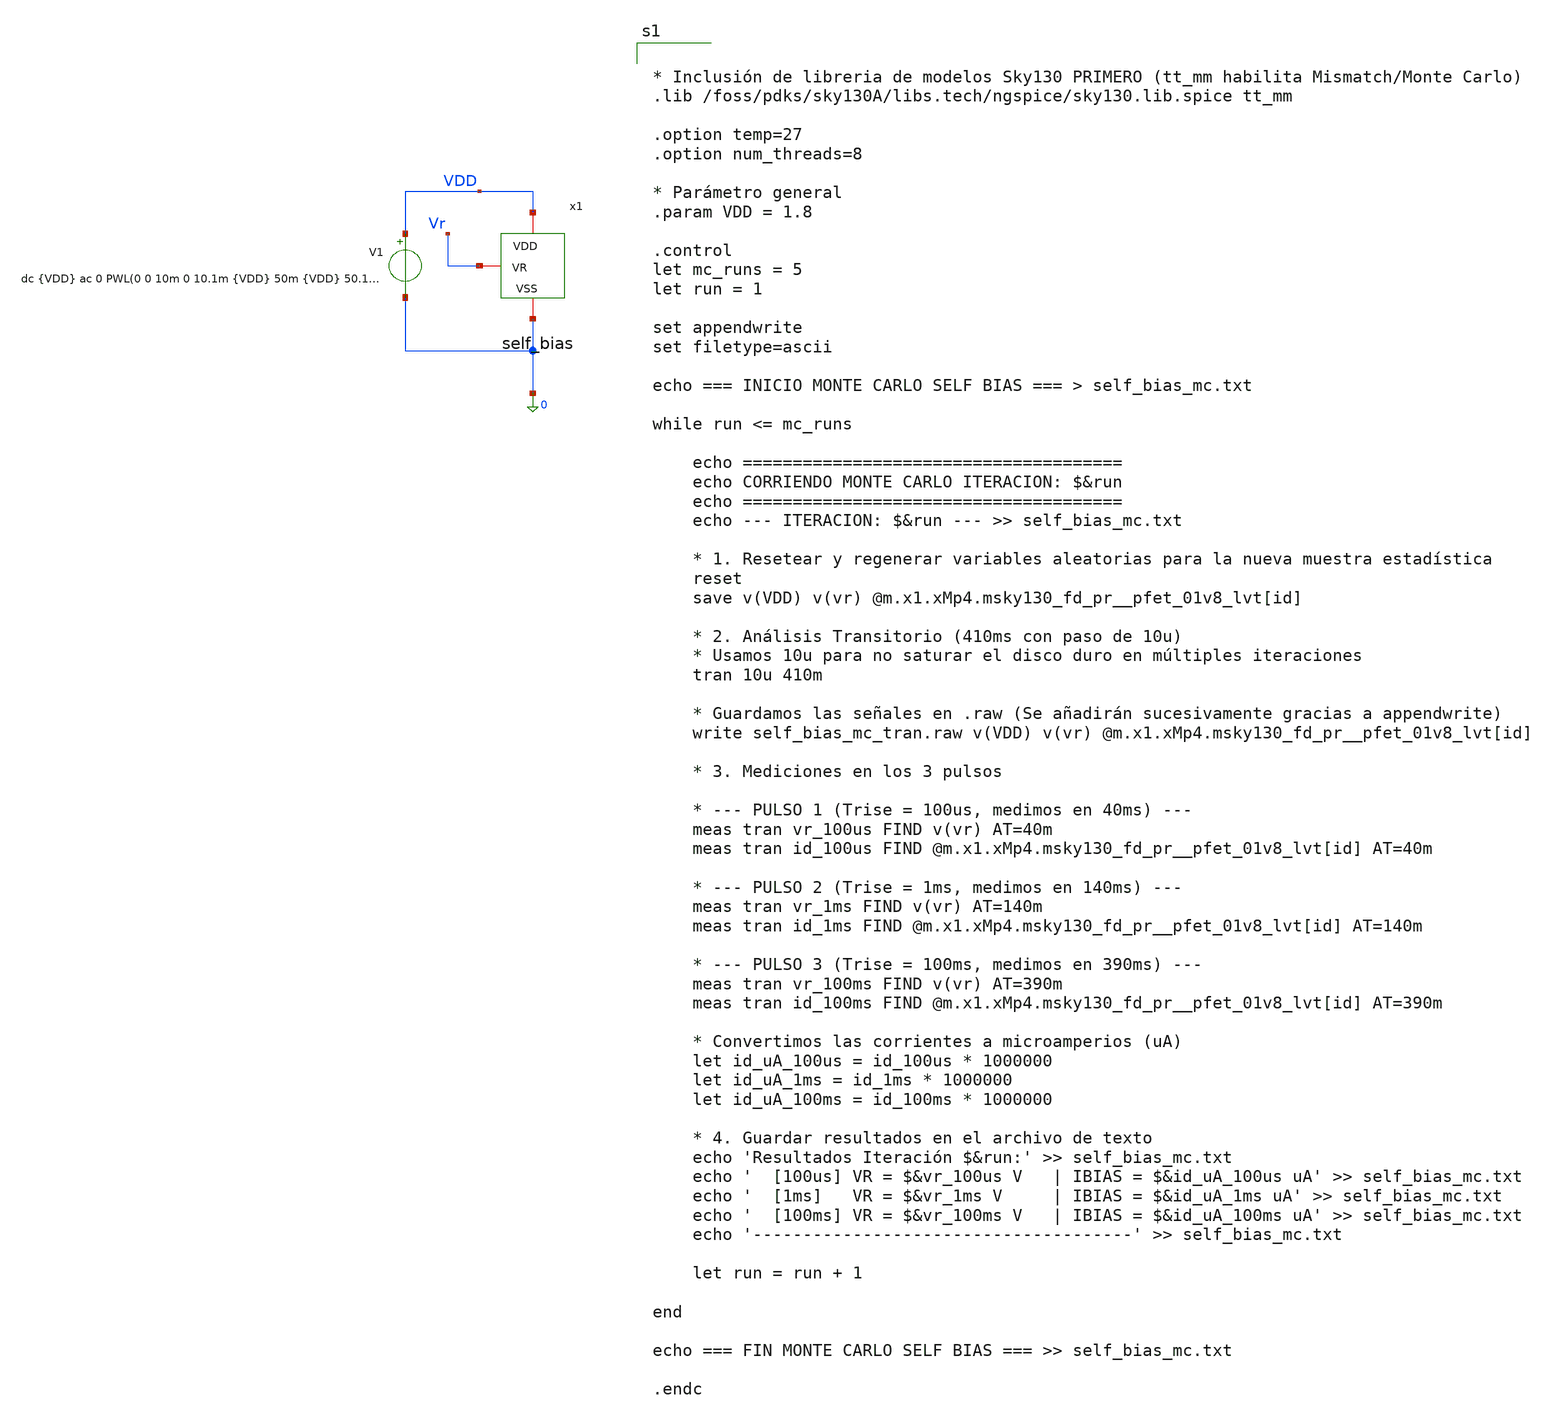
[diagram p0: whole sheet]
** sch_path: xschem/Iref/self_bias_tb_mc.sch
**.subckt self_bias_tb_mc
V1 VDD 0 dc {VDD} ac 0 PWL(0 0 10m 0 10.1m {VDD} 50m {VDD} 50.1m 0 100m 0 101m {VDD} 150m {VDD} 150.1m
+ 0 200m 0 300m {VDD} 400m {VDD} 400.1m 0)
x1 VDD Vr 0 self_bias
**** begin user architecture code


* Inclusión de libreria de modelos Sky130 PRIMERO (tt_mm habilita Mismatch/Monte Carlo)
.lib /foss/pdks/sky130A/libs.tech/ngspice/sky130.lib.spice tt_mm

.option temp=27
.option num_threads=8

* Parámetro general
.param VDD = 1.8

.control
let mc_runs = 5
let run = 1

set appendwrite
set filetype=ascii

echo === INICIO MONTE CARLO SELF BIAS === > self_bias_mc.txt

while run <= mc_runs

    echo ======================================
    echo CORRIENDO MONTE CARLO ITERACION: $&run
    echo ======================================
    echo --- ITERACION: $&run --- >> self_bias_mc.txt

    * 1. Resetear y regenerar variables aleatorias para la nueva muestra estadística
    reset
    save v(VDD) v(vr) @m.x1.xMp4.msky130_fd_pr__pfet_01v8_lvt[id]

    * 2. Análisis Transitorio (410ms con paso de 10u)
    * Usamos 10u para no saturar el disco duro en múltiples iteraciones
    tran 10u 410m

    * Guardamos las señales en .raw (Se añadirán sucesivamente gracias a appendwrite)
    write self_bias_mc_tran.raw v(VDD) v(vr) @m.x1.xMp4.msky130_fd_pr__pfet_01v8_lvt[id]

    * 3. Mediciones en los 3 pulsos

    * --- PULSO 1 (Trise = 100us, medimos en 40ms) ---
    meas tran vr_100us FIND v(vr) AT=40m
    meas tran id_100us FIND @m.x1.xMp4.msky130_fd_pr__pfet_01v8_lvt[id] AT=40m

    * --- PULSO 2 (Trise = 1ms, medimos en 140ms) ---
    meas tran vr_1ms FIND v(vr) AT=140m
    meas tran id_1ms FIND @m.x1.xMp4.msky130_fd_pr__pfet_01v8_lvt[id] AT=140m

    * --- PULSO 3 (Trise = 100ms, medimos en 390ms) ---
    meas tran vr_100ms FIND v(vr) AT=390m
    meas tran id_100ms FIND @m.x1.xMp4.msky130_fd_pr__pfet_01v8_lvt[id] AT=390m

    * Convertimos las corrientes a microamperios (uA)
    let id_uA_100us = id_100us * 1000000
    let id_uA_1ms = id_1ms * 1000000
    let id_uA_100ms = id_100ms * 1000000

    * 4. Guardar resultados en el archivo de texto
    echo 'Resultados Iteración $&run:' >> self_bias_mc.txt
    echo '  [100us] VR = $&vr_100us V   | IBIAS = $&id_uA_100us uA' >> self_bias_mc.txt
    echo '  [1ms]   VR = $&vr_1ms V     | IBIAS = $&id_uA_1ms uA' >> self_bias_mc.txt
    echo '  [100ms] VR = $&vr_100ms V   | IBIAS = $&id_uA_100ms uA' >> self_bias_mc.txt
    echo '--------------------------------------' >> self_bias_mc.txt

    let run = run + 1

end

echo === FIN MONTE CARLO SELF BIAS === >> self_bias_mc.txt

.endc


**** end user architecture code
**.ends

* expanding   symbol:  self_bias.sym # of pins=3
** sym_path: xschem/Iref/self_bias.sym
** sch_path: xschem/Iref/self_bias.sch
.subckt self_bias VDD VR VSS
*.iopin VR
*.iopin VDD
*.iopin VSS
XMp4 vgp_self vgp_self VDD VDD sky130_fd_pr__pfet_01v8_lvt L=1 W=30 nf=6 ad='int((6 + 1)/2) * 30 / 6 * 0.29'
+ as='int((6 + 2)/2) * 30 / 6 * 0.29' pd='2*int((6 + 1)/2) * (30 / 6 + 0.29)' ps='2*int((6 + 2)/2) * (30 / 6 + 0.29)'
+ nrd='0.29 / 30 ' nrs='0.29 / 30 ' sa=0 sb=0 sd=0 mult=1 m=1
XMp3 VDI vgp_self VDD VDD sky130_fd_pr__pfet_01v8_lvt L=1 W=30 nf=6 ad='int((6 + 1)/2) * 30 / 6 * 0.29'
+ as='int((6 + 2)/2) * 30 / 6 * 0.29' pd='2*int((6 + 1)/2) * (30 / 6 + 0.29)' ps='2*int((6 + 2)/2) * (30 / 6 + 0.29)'
+ nrd='0.29 / 30 ' nrs='0.29 / 30 ' sa=0 sb=0 sd=0 mult=1 m=1
XMs2 VDinv VR vp1 VDD sky130_fd_pr__pfet_01v8_lvt L=5 W=0.5 nf=1 ad='int((1 + 1)/2) * 0.5 / 1 * 0.29'
+ as='int((1 + 2)/2) * 0.5 / 1 * 0.29' pd='2*int((1 + 1)/2) * (0.5 / 1 + 0.29)' ps='2*int((1 + 2)/2) * (0.5 / 1 + 0.29)'
+ nrd='0.29 / 0.5 ' nrs='0.29 / 0.5 ' sa=0 sb=0 sd=0 mult=1 m=1
XMn2 vgp_self VDI VR VSS sky130_fd_pr__nfet_01v8 L=1 W=24 nf=6 ad='int((6 + 1)/2) * 24 / 6 * 0.29' as='int((6 + 2)/2) * 24 / 6 * 0.29'
+ pd='2*int((6 + 1)/2) * (24 / 6 + 0.29)' ps='2*int((6 + 2)/2) * (24 / 6 + 0.29)' nrd='0.29 / 24 ' nrs='0.29 / 24 '
+ sa=0 sb=0 sd=0 mult=1 m=1
XMn1 VDI VR VSS VSS sky130_fd_pr__nfet_01v8 L=1 W=5 nf=5 ad='int((5 + 1)/2) * 5 / 5 * 0.29' as='int((5 + 2)/2) * 5 / 5 * 0.29'
+ pd='2*int((5 + 1)/2) * (5 / 5 + 0.29)' ps='2*int((5 + 2)/2) * (5 / 5 + 0.29)' nrd='0.29 / 5 ' nrs='0.29 / 5 '
+ sa=0 sb=0 sd=0 mult=1 m=1
XMs3 VDinv VR VSS VSS sky130_fd_pr__nfet_01v8 L=1 W=20 nf=5 ad='int((5 + 1)/2) * 20 / 5 * 0.29' as='int((5 + 2)/2) * 20 / 5 * 0.29'
+ pd='2*int((5 + 1)/2) * (20 / 5 + 0.29)' ps='2*int((5 + 2)/2) * (20 / 5 + 0.29)' nrd='0.29 / 20 ' nrs='0.29 / 20 '
+ sa=0 sb=0 sd=0 mult=1 m=1
XMs1 vgp_self VDinv VSS VSS sky130_fd_pr__nfet_01v8 L=1 W=2 nf=2 ad='int((2 + 1)/2) * 2 / 2 * 0.29' as='int((2 + 2)/2) * 2 / 2 * 0.29'
+ pd='2*int((2 + 1)/2) * (2 / 2 + 0.29)' ps='2*int((2 + 2)/2) * (2 / 2 + 0.29)' nrd='0.29 / 2 ' nrs='0.29 / 2 '
+ sa=0 sb=0 sd=0 mult=1 m=1
XR11 VSS VR VSS sky130_fd_pr__res_xhigh_po_0p69 L=20.7 mult=1 m=1
XMs4 vp1 VR vp2 VDD sky130_fd_pr__pfet_01v8_lvt L=5 W=0.5 nf=1 ad='int((1 + 1)/2) * 0.5 / 1 * 0.29' as='int((1 + 2)/2) * 0.5 / 1 * 0.29'
+ pd='2*int((1 + 1)/2) * (0.5 / 1 + 0.29)' ps='2*int((1 + 2)/2) * (0.5 / 1 + 0.29)' nrd='0.29 / 0.5 ' nrs='0.29 / 0.5 '
+ sa=0 sb=0 sd=0 mult=1 m=1
XMs5 vp2 VR vp3 VDD sky130_fd_pr__pfet_01v8_lvt L=5 W=0.5 nf=1 ad='int((1 + 1)/2) * 0.5 / 1 * 0.29' as='int((1 + 2)/2) * 0.5 / 1 * 0.29'
+ pd='2*int((1 + 1)/2) * (0.5 / 1 + 0.29)' ps='2*int((1 + 2)/2) * (0.5 / 1 + 0.29)' nrd='0.29 / 0.5 ' nrs='0.29 / 0.5 '
+ sa=0 sb=0 sd=0 mult=1 m=1
XMs6 vp3 VR vp4 VDD sky130_fd_pr__pfet_01v8_lvt L=5 W=0.5 nf=1 ad='int((1 + 1)/2) * 0.5 / 1 * 0.29' as='int((1 + 2)/2) * 0.5 / 1 * 0.29'
+ pd='2*int((1 + 1)/2) * (0.5 / 1 + 0.29)' ps='2*int((1 + 2)/2) * (0.5 / 1 + 0.29)' nrd='0.29 / 0.5 ' nrs='0.29 / 0.5 '
+ sa=0 sb=0 sd=0 mult=1 m=1
XMs7 vp4 VR VDD VDD sky130_fd_pr__pfet_01v8_lvt L=5 W=0.5 nf=1 ad='int((1 + 1)/2) * 0.5 / 1 * 0.29' as='int((1 + 2)/2) * 0.5 / 1 * 0.29'
+ pd='2*int((1 + 1)/2) * (0.5 / 1 + 0.29)' ps='2*int((1 + 2)/2) * (0.5 / 1 + 0.29)' nrd='0.29 / 0.5 ' nrs='0.29 / 0.5 '
+ sa=0 sb=0 sd=0 mult=1 m=1
.ends

.end
